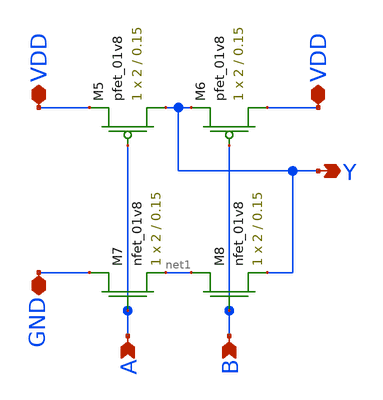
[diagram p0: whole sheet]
** sch_path: schematic/layout_driven_schematics/nand2.sch
**.subckt nand2 A Y B VDD VDD GND
*.ipin A
*.opin Y
*.ipin B
*.iopin VDD
*.iopin VDD
*.iopin GND
XM5 Y A VDD VDD sky130_fd_pr__pfet_01v8 L=0.15 W=2 nf=1 ad='int((nf+1)/2) * W/nf * 0.29' as='int((nf+2)/2) * W/nf * 0.29'
+ pd='2*int((nf+1)/2) * (W/nf + 0.29)' ps='2*int((nf+2)/2) * (W/nf + 0.29)' nrd='0.29 / W' nrs='0.29 / W'
+ sa=0 sb=0 sd=0 mult=1 m=1
XM6 VDD B Y VDD sky130_fd_pr__pfet_01v8 L=0.15 W=2 nf=1 ad='int((nf+1)/2) * W/nf * 0.29' as='int((nf+2)/2) * W/nf * 0.29'
+ pd='2*int((nf+1)/2) * (W/nf + 0.29)' ps='2*int((nf+2)/2) * (W/nf + 0.29)' nrd='0.29 / W' nrs='0.29 / W'
+ sa=0 sb=0 sd=0 mult=1 m=1
XM7 GND A net1 GND sky130_fd_pr__nfet_01v8 L=0.15 W=2 nf=1 ad='int((nf+1)/2) * W/nf * 0.29' as='int((nf+2)/2) * W/nf * 0.29'
+ pd='2*int((nf+1)/2) * (W/nf + 0.29)' ps='2*int((nf+2)/2) * (W/nf + 0.29)' nrd='0.29 / W' nrs='0.29 / W'
+ sa=0 sb=0 sd=0 mult=1 m=1
XM8 net1 B Y GND sky130_fd_pr__nfet_01v8 L=0.15 W=2 nf=1 ad='int((nf+1)/2) * W/nf * 0.29' as='int((nf+2)/2) * W/nf * 0.29'
+ pd='2*int((nf+1)/2) * (W/nf + 0.29)' ps='2*int((nf+2)/2) * (W/nf + 0.29)' nrd='0.29 / W' nrs='0.29 / W'
+ sa=0 sb=0 sd=0 mult=1 m=1
**.ends
.end
